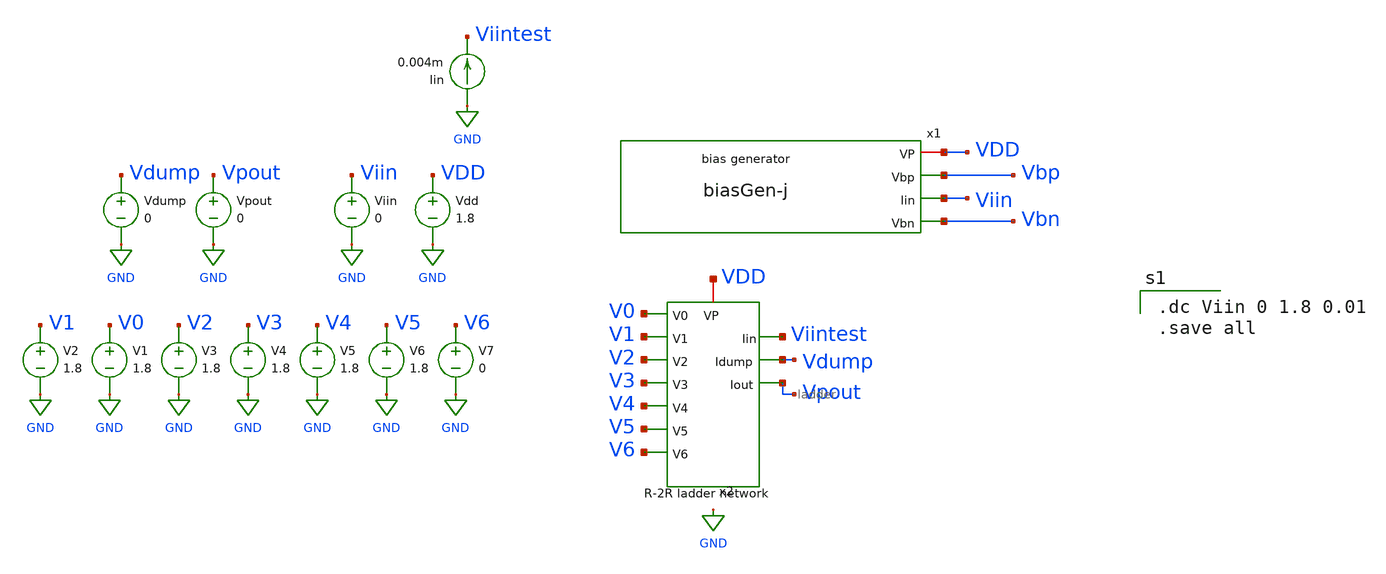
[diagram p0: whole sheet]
** sch_path: xschem/test_cur_gen_sim.sch
**.subckt test_cur_gen_sim
x1 VDD Vbp Viin Vbn biasGen-j
Vdd VDD GND 1.8
Viin Viin GND 0
V1 V0 GND 1.8
Iin GND Viintest 0.004m
Vpout Vpout GND 0
V2 V1 GND 1.8
V3 V2 GND 1.8
V4 V3 GND 1.8
V5 V4 GND 1.8
V6 V5 GND 1.8
V7 V6 GND 0
Vdump Vdump GND 0
x2 V0 VDD Vdump Vpout Viintest V1 V2 V3 V4 V5 V6 ladder
**** begin user architecture code

.option wnflag=1
.param MC_SWITCH=0.0
.lib ~/skywater/skywater-pdk/libraries/sky130_fd_pr_ngspice/latest/models/sky130.lib.spice tt


.dc Viin 0 1.8 0.01
.save all

**** end user architecture code
**.ends

* expanding   symbol:  ./biasGen-j.sym # of pins=4
** sym_path: xschem/biasGen-j.sym
** sch_path: xschem/biasGen-j.sch
.subckt biasGen-j VP Vbp Iin Vbn
*.opin Iin
*.opin Vbp
*.opin Vbn
*.iopin VP
XM1 Vbn Vbn GND GND sky130_fd_pr__nfet_01v8 L=4 W=12 nf=1 ad='int((nf+1)/2) * W/nf * 0.29' as='int((nf+2)/2) * W/nf * 0.29'
+ pd='2*int((nf+1)/2) * (W/nf + 0.29)' ps='2*int((nf+2)/2) * (W/nf + 0.29)' nrd='0.29 / W' nrs='0.29 / W'
+ sa=0 sb=0 sd=0 mult=1 m=1
XM2 GND Vbn Vbp GND sky130_fd_pr__nfet_01v8 L=4 W=12 nf=1 ad='int((nf+1)/2) * W/nf * 0.29' as='int((nf+2)/2) * W/nf * 0.29'
+ pd='2*int((nf+1)/2) * (W/nf + 0.29)' ps='2*int((nf+2)/2) * (W/nf + 0.29)' nrd='0.29 / W' nrs='0.29 / W'
+ sa=0 sb=0 sd=0 mult=1 m=1
XM3 net1 net2 GND GND sky130_fd_pr__nfet_01v8 L=4 W=12 nf=1 ad='int((nf+1)/2) * W/nf * 0.29' as='int((nf+2)/2) * W/nf * 0.29'
+ pd='2*int((nf+1)/2) * (W/nf + 0.29)' ps='2*int((nf+2)/2) * (W/nf + 0.29)' nrd='0.29 / W' nrs='0.29 / W'
+ sa=0 sb=0 sd=0 mult=1 m=1
XM4 net3 net2 net2 GND sky130_fd_pr__nfet_01v8 L=4 W=96 nf=1 ad='int((nf+1)/2) * W/nf * 0.29' as='int((nf+2)/2) * W/nf * 0.29'
+ pd='2*int((nf+1)/2) * (W/nf + 0.29)' ps='2*int((nf+2)/2) * (W/nf + 0.29)' nrd='0.29 / W' nrs='0.29 / W'
+ sa=0 sb=0 sd=0 mult=1 m=1
XM5 Vbp net1 VP VDD sky130_fd_pr__pfet_01v8 L=4 W=12 nf=1 ad='int((nf+1)/2) * W/nf * 0.29' as='int((nf+2)/2) * W/nf * 0.29'
+ pd='2*int((nf+1)/2) * (W/nf + 0.29)' ps='2*int((nf+2)/2) * (W/nf + 0.29)' nrd='0.29 / W' nrs='0.29 / W'
+ sa=0 sb=0 sd=0 mult=1 m=1
XM6 VP net1 net1 VDD sky130_fd_pr__pfet_01v8 L=4 W=12 nf=1 ad='int((nf+1)/2) * W/nf * 0.29' as='int((nf+2)/2) * W/nf * 0.29'
+ pd='2*int((nf+1)/2) * (W/nf + 0.29)' ps='2*int((nf+2)/2) * (W/nf + 0.29)' nrd='0.29 / W' nrs='0.29 / W'
+ sa=0 sb=0 sd=0 mult=1 m=1
XM7 VP Vbp net2 VDD sky130_fd_pr__pfet_01v8 L=4 W=12 nf=1 ad='int((nf+1)/2) * W/nf * 0.29' as='int((nf+2)/2) * W/nf * 0.29'
+ pd='2*int((nf+1)/2) * (W/nf + 0.29)' ps='2*int((nf+2)/2) * (W/nf + 0.29)' nrd='0.29 / W' nrs='0.29 / W'
+ sa=0 sb=0 sd=0 mult=1 m=1
XM8 Vbn Vbp VP VDD sky130_fd_pr__pfet_01v8 L=4 W=12 nf=1 ad='int((nf+1)/2) * W/nf * 0.29' as='int((nf+2)/2) * W/nf * 0.29'
+ pd='2*int((nf+1)/2) * (W/nf + 0.29)' ps='2*int((nf+2)/2) * (W/nf + 0.29)' nrd='0.29 / W' nrs='0.29 / W'
+ sa=0 sb=0 sd=0 mult=1 m=1
R1 net3 GND 50k m=1
XM9 Iin Vbp VP VDD sky130_fd_pr__pfet_01v8 L=4 W=12 nf=1 ad='int((nf+1)/2) * W/nf * 0.29' as='int((nf+2)/2) * W/nf * 0.29'
+ pd='2*int((nf+1)/2) * (W/nf + 0.29)' ps='2*int((nf+2)/2) * (W/nf + 0.29)' nrd='0.29 / W' nrs='0.29 / W'
+ sa=0 sb=0 sd=0 mult=1 m=1
.ends


* expanding   symbol:  /home/madvlsi/Documents/MP4/DAC-VLSI/xschem/ladder.sym # of pins=11
** sym_path: /home/madvlsi/Documents/MP4/DAC-VLSI/xschem/ladder.sym
** sch_path: /home/madvlsi/Documents/MP4/DAC-VLSI/xschem/ladder.sch
.subckt ladder V0 VP Idump Iout Iin V1 V2 V3 V4 V5 V6
*.ipin V6
*.ipin V5
*.ipin V4
*.ipin V3
*.ipin V2
*.ipin V1
*.ipin V0
*.iopin VP
*.iopin Iin
*.opin Idump
*.opin Iout
XM1 Iin VP net1 GND sky130_fd_pr__nfet_01v8 L=4 W=12 nf=1 ad='int((nf+1)/2) * W/nf * 0.29' as='int((nf+2)/2) * W/nf * 0.29'
+ pd='2*int((nf+1)/2) * (W/nf + 0.29)' ps='2*int((nf+2)/2) * (W/nf + 0.29)' nrd='0.29 / W' nrs='0.29 / W'
+ sa=0 sb=0 sd=0 mult=1 m=1
XM3 Iin VP net2 GND sky130_fd_pr__nfet_01v8 L=4 W=12 nf=1 ad='int((nf+1)/2) * W/nf * 0.29' as='int((nf+2)/2) * W/nf * 0.29'
+ pd='2*int((nf+1)/2) * (W/nf + 0.29)' ps='2*int((nf+2)/2) * (W/nf + 0.29)' nrd='0.29 / W' nrs='0.29 / W'
+ sa=0 sb=0 sd=0 mult=1 m=1
XM5 net2 VP net3 GND sky130_fd_pr__nfet_01v8 L=4 W=12 nf=1 ad='int((nf+1)/2) * W/nf * 0.29' as='int((nf+2)/2) * W/nf * 0.29'
+ pd='2*int((nf+1)/2) * (W/nf + 0.29)' ps='2*int((nf+2)/2) * (W/nf + 0.29)' nrd='0.29 / W' nrs='0.29 / W'
+ sa=0 sb=0 sd=0 mult=1 m=1
XM7 net2 VP net4 GND sky130_fd_pr__nfet_01v8 L=4 W=12 nf=1 ad='int((nf+1)/2) * W/nf * 0.29' as='int((nf+2)/2) * W/nf * 0.29'
+ pd='2*int((nf+1)/2) * (W/nf + 0.29)' ps='2*int((nf+2)/2) * (W/nf + 0.29)' nrd='0.29 / W' nrs='0.29 / W'
+ sa=0 sb=0 sd=0 mult=1 m=1
XM6 net3 V5 Iout GND sky130_fd_pr__nfet_01v8 L=4 W=12 nf=1 ad='int((nf+1)/2) * W/nf * 0.29' as='int((nf+2)/2) * W/nf * 0.29'
+ pd='2*int((nf+1)/2) * (W/nf + 0.29)' ps='2*int((nf+2)/2) * (W/nf + 0.29)' nrd='0.29 / W' nrs='0.29 / W'
+ sa=0 sb=0 sd=0 mult=1 m=1
XM8 net3 net16 Idump GND sky130_fd_pr__nfet_01v8 L=4 W=12 nf=1 ad='int((nf+1)/2) * W/nf * 0.29' as='int((nf+2)/2) * W/nf * 0.29'
+ pd='2*int((nf+1)/2) * (W/nf + 0.29)' ps='2*int((nf+2)/2) * (W/nf + 0.29)' nrd='0.29 / W' nrs='0.29 / W'
+ sa=0 sb=0 sd=0 mult=1 m=1
XM2 net1 V6 Iout GND sky130_fd_pr__nfet_01v8 L=4 W=12 nf=1 ad='int((nf+1)/2) * W/nf * 0.29' as='int((nf+2)/2) * W/nf * 0.29'
+ pd='2*int((nf+1)/2) * (W/nf + 0.29)' ps='2*int((nf+2)/2) * (W/nf + 0.29)' nrd='0.29 / W' nrs='0.29 / W'
+ sa=0 sb=0 sd=0 mult=1 m=1
XM4 net1 net15 Idump GND sky130_fd_pr__nfet_01v8 L=4 W=12 nf=1 ad='int((nf+1)/2) * W/nf * 0.29' as='int((nf+2)/2) * W/nf * 0.29'
+ pd='2*int((nf+1)/2) * (W/nf + 0.29)' ps='2*int((nf+2)/2) * (W/nf + 0.29)' nrd='0.29 / W' nrs='0.29 / W'
+ sa=0 sb=0 sd=0 mult=1 m=1
XM9 net4 VP net5 GND sky130_fd_pr__nfet_01v8 L=4 W=12 nf=1 ad='int((nf+1)/2) * W/nf * 0.29' as='int((nf+2)/2) * W/nf * 0.29'
+ pd='2*int((nf+1)/2) * (W/nf + 0.29)' ps='2*int((nf+2)/2) * (W/nf + 0.29)' nrd='0.29 / W' nrs='0.29 / W'
+ sa=0 sb=0 sd=0 mult=1 m=1
XM11 net4 VP net6 GND sky130_fd_pr__nfet_01v8 L=4 W=12 nf=1 ad='int((nf+1)/2) * W/nf * 0.29' as='int((nf+2)/2) * W/nf * 0.29'
+ pd='2*int((nf+1)/2) * (W/nf + 0.29)' ps='2*int((nf+2)/2) * (W/nf + 0.29)' nrd='0.29 / W' nrs='0.29 / W'
+ sa=0 sb=0 sd=0 mult=1 m=1
XM10 net5 V4 Iout GND sky130_fd_pr__nfet_01v8 L=4 W=12 nf=1 ad='int((nf+1)/2) * W/nf * 0.29' as='int((nf+2)/2) * W/nf * 0.29'
+ pd='2*int((nf+1)/2) * (W/nf + 0.29)' ps='2*int((nf+2)/2) * (W/nf + 0.29)' nrd='0.29 / W' nrs='0.29 / W'
+ sa=0 sb=0 sd=0 mult=1 m=1
XM12 net5 net17 Idump GND sky130_fd_pr__nfet_01v8 L=4 W=12 nf=1 ad='int((nf+1)/2) * W/nf * 0.29' as='int((nf+2)/2) * W/nf * 0.29'
+ pd='2*int((nf+1)/2) * (W/nf + 0.29)' ps='2*int((nf+2)/2) * (W/nf + 0.29)' nrd='0.29 / W' nrs='0.29 / W'
+ sa=0 sb=0 sd=0 mult=1 m=1
XM13 net6 VP net7 GND sky130_fd_pr__nfet_01v8 L=4 W=12 nf=1 ad='int((nf+1)/2) * W/nf * 0.29' as='int((nf+2)/2) * W/nf * 0.29'
+ pd='2*int((nf+1)/2) * (W/nf + 0.29)' ps='2*int((nf+2)/2) * (W/nf + 0.29)' nrd='0.29 / W' nrs='0.29 / W'
+ sa=0 sb=0 sd=0 mult=1 m=1
XM15 net6 VP net8 GND sky130_fd_pr__nfet_01v8 L=4 W=12 nf=1 ad='int((nf+1)/2) * W/nf * 0.29' as='int((nf+2)/2) * W/nf * 0.29'
+ pd='2*int((nf+1)/2) * (W/nf + 0.29)' ps='2*int((nf+2)/2) * (W/nf + 0.29)' nrd='0.29 / W' nrs='0.29 / W'
+ sa=0 sb=0 sd=0 mult=1 m=1
XM14 net7 V3 Iout GND sky130_fd_pr__nfet_01v8 L=4 W=12 nf=1 ad='int((nf+1)/2) * W/nf * 0.29' as='int((nf+2)/2) * W/nf * 0.29'
+ pd='2*int((nf+1)/2) * (W/nf + 0.29)' ps='2*int((nf+2)/2) * (W/nf + 0.29)' nrd='0.29 / W' nrs='0.29 / W'
+ sa=0 sb=0 sd=0 mult=1 m=1
XM16 net7 net18 Idump GND sky130_fd_pr__nfet_01v8 L=4 W=12 nf=1 ad='int((nf+1)/2) * W/nf * 0.29' as='int((nf+2)/2) * W/nf * 0.29'
+ pd='2*int((nf+1)/2) * (W/nf + 0.29)' ps='2*int((nf+2)/2) * (W/nf + 0.29)' nrd='0.29 / W' nrs='0.29 / W'
+ sa=0 sb=0 sd=0 mult=1 m=1
XM17 net8 VP net9 GND sky130_fd_pr__nfet_01v8 L=4 W=12 nf=1 ad='int((nf+1)/2) * W/nf * 0.29' as='int((nf+2)/2) * W/nf * 0.29'
+ pd='2*int((nf+1)/2) * (W/nf + 0.29)' ps='2*int((nf+2)/2) * (W/nf + 0.29)' nrd='0.29 / W' nrs='0.29 / W'
+ sa=0 sb=0 sd=0 mult=1 m=1
XM19 net8 VP net10 GND sky130_fd_pr__nfet_01v8 L=4 W=12 nf=1 ad='int((nf+1)/2) * W/nf * 0.29' as='int((nf+2)/2) * W/nf * 0.29'
+ pd='2*int((nf+1)/2) * (W/nf + 0.29)' ps='2*int((nf+2)/2) * (W/nf + 0.29)' nrd='0.29 / W' nrs='0.29 / W'
+ sa=0 sb=0 sd=0 mult=1 m=1
XM18 net9 V2 Iout GND sky130_fd_pr__nfet_01v8 L=4 W=12 nf=1 ad='int((nf+1)/2) * W/nf * 0.29' as='int((nf+2)/2) * W/nf * 0.29'
+ pd='2*int((nf+1)/2) * (W/nf + 0.29)' ps='2*int((nf+2)/2) * (W/nf + 0.29)' nrd='0.29 / W' nrs='0.29 / W'
+ sa=0 sb=0 sd=0 mult=1 m=1
XM20 net9 net19 Idump GND sky130_fd_pr__nfet_01v8 L=4 W=12 nf=1 ad='int((nf+1)/2) * W/nf * 0.29' as='int((nf+2)/2) * W/nf * 0.29'
+ pd='2*int((nf+1)/2) * (W/nf + 0.29)' ps='2*int((nf+2)/2) * (W/nf + 0.29)' nrd='0.29 / W' nrs='0.29 / W'
+ sa=0 sb=0 sd=0 mult=1 m=1
XM21 net10 VP net11 GND sky130_fd_pr__nfet_01v8 L=4 W=12 nf=1 ad='int((nf+1)/2) * W/nf * 0.29' as='int((nf+2)/2) * W/nf * 0.29'
+ pd='2*int((nf+1)/2) * (W/nf + 0.29)' ps='2*int((nf+2)/2) * (W/nf + 0.29)' nrd='0.29 / W' nrs='0.29 / W'
+ sa=0 sb=0 sd=0 mult=1 m=1
XM23 net10 VP net12 GND sky130_fd_pr__nfet_01v8 L=4 W=12 nf=1 ad='int((nf+1)/2) * W/nf * 0.29' as='int((nf+2)/2) * W/nf * 0.29'
+ pd='2*int((nf+1)/2) * (W/nf + 0.29)' ps='2*int((nf+2)/2) * (W/nf + 0.29)' nrd='0.29 / W' nrs='0.29 / W'
+ sa=0 sb=0 sd=0 mult=1 m=1
XM22 net11 V1 Iout GND sky130_fd_pr__nfet_01v8 L=4 W=12 nf=1 ad='int((nf+1)/2) * W/nf * 0.29' as='int((nf+2)/2) * W/nf * 0.29'
+ pd='2*int((nf+1)/2) * (W/nf + 0.29)' ps='2*int((nf+2)/2) * (W/nf + 0.29)' nrd='0.29 / W' nrs='0.29 / W'
+ sa=0 sb=0 sd=0 mult=1 m=1
XM24 net11 net20 Idump GND sky130_fd_pr__nfet_01v8 L=4 W=12 nf=1 ad='int((nf+1)/2) * W/nf * 0.29' as='int((nf+2)/2) * W/nf * 0.29'
+ pd='2*int((nf+1)/2) * (W/nf + 0.29)' ps='2*int((nf+2)/2) * (W/nf + 0.29)' nrd='0.29 / W' nrs='0.29 / W'
+ sa=0 sb=0 sd=0 mult=1 m=1
XM25 net12 VP net13 GND sky130_fd_pr__nfet_01v8 L=4 W=12 nf=1 ad='int((nf+1)/2) * W/nf * 0.29' as='int((nf+2)/2) * W/nf * 0.29'
+ pd='2*int((nf+1)/2) * (W/nf + 0.29)' ps='2*int((nf+2)/2) * (W/nf + 0.29)' nrd='0.29 / W' nrs='0.29 / W'
+ sa=0 sb=0 sd=0 mult=1 m=1
XM27 net12 VP net14 GND sky130_fd_pr__nfet_01v8 L=4 W=12 nf=1 ad='int((nf+1)/2) * W/nf * 0.29' as='int((nf+2)/2) * W/nf * 0.29'
+ pd='2*int((nf+1)/2) * (W/nf + 0.29)' ps='2*int((nf+2)/2) * (W/nf + 0.29)' nrd='0.29 / W' nrs='0.29 / W'
+ sa=0 sb=0 sd=0 mult=1 m=1
XM26 net13 V0 Iout GND sky130_fd_pr__nfet_01v8 L=4 W=12 nf=1 ad='int((nf+1)/2) * W/nf * 0.29' as='int((nf+2)/2) * W/nf * 0.29'
+ pd='2*int((nf+1)/2) * (W/nf + 0.29)' ps='2*int((nf+2)/2) * (W/nf + 0.29)' nrd='0.29 / W' nrs='0.29 / W'
+ sa=0 sb=0 sd=0 mult=1 m=1
XM28 net13 net21 Idump GND sky130_fd_pr__nfet_01v8 L=4 W=12 nf=1 ad='int((nf+1)/2) * W/nf * 0.29' as='int((nf+2)/2) * W/nf * 0.29'
+ pd='2*int((nf+1)/2) * (W/nf + 0.29)' ps='2*int((nf+2)/2) * (W/nf + 0.29)' nrd='0.29 / W' nrs='0.29 / W'
+ sa=0 sb=0 sd=0 mult=1 m=1
XM29 net14 VP Idump GND sky130_fd_pr__nfet_01v8 L=4 W=12 nf=1 ad='int((nf+1)/2) * W/nf * 0.29' as='int((nf+2)/2) * W/nf * 0.29'
+ pd='2*int((nf+1)/2) * (W/nf + 0.29)' ps='2*int((nf+2)/2) * (W/nf + 0.29)' nrd='0.29 / W' nrs='0.29 / W'
+ sa=0 sb=0 sd=0 mult=1 m=1
x1 net15 V6 inverter
x2 net16 V5 inverter
x3 net17 V4 inverter
x4 net18 V3 inverter
x5 net19 V2 inverter
x6 net20 V1 inverter
x7 net21 V0 inverter
.ends


* expanding   symbol:  ./inverter.sym # of pins=2
** sym_path: xschem/inverter.sym
** sch_path: xschem/inverter.sch
.subckt inverter Y A
*.ipin A
*.opin Y
XM1 Y A VDD VDD sky130_fd_pr__pfet_01v8 L=0.15 W=1 nf=1 ad='int((nf+1)/2) * W/nf * 0.29' as='int((nf+2)/2) * W/nf * 0.29'
+ pd='2*int((nf+1)/2) * (W/nf + 0.29)' ps='2*int((nf+2)/2) * (W/nf + 0.29)' nrd='0.29 / W' nrs='0.29 / W'
+ sa=0 sb=0 sd=0 mult=1 m=1
XM2 Y A GND GND sky130_fd_pr__nfet_01v8 L=0.15 W=1 nf=1 ad='int((nf+1)/2) * W/nf * 0.29' as='int((nf+2)/2) * W/nf * 0.29'
+ pd='2*int((nf+1)/2) * (W/nf + 0.29)' ps='2*int((nf+2)/2) * (W/nf + 0.29)' nrd='0.29 / W' nrs='0.29 / W'
+ sa=0 sb=0 sd=0 mult=1 m=1
.ends

.GLOBAL GND
.GLOBAL VDD
.end
